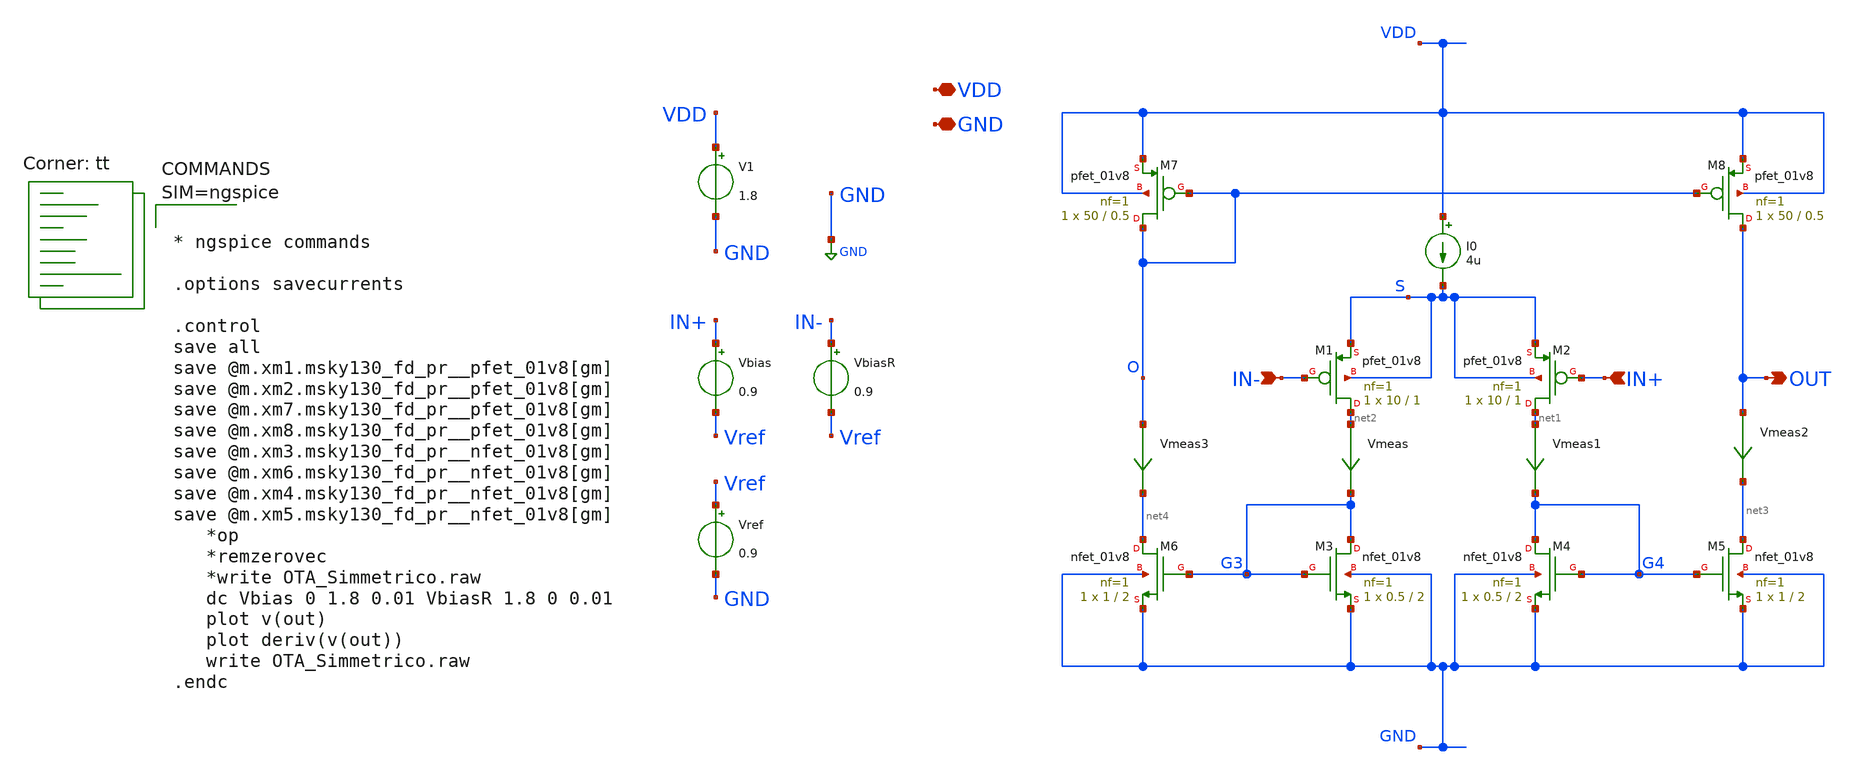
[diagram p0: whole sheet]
** sch_path: xschem/OTA_Simmetrico.sch
**.subckt OTA_Simmetrico VDD GND IN+ IN- OUT
*.iopin VDD
*.iopin GND
*.ipin IN+
*.ipin IN-
*.opin OUT
XM1 net2 IN- S S sky130_fd_pr__pfet_01v8 L=1 W=10 nf=1 ad='int((nf+1)/2) * W/nf * 0.29' as='int((nf+2)/2) * W/nf * 0.29'
+ pd='2*int((nf+1)/2) * (W/nf + 0.29)' ps='2*int((nf+2)/2) * (W/nf + 0.29)' nrd='0.29 / W' nrs='0.29 / W'
+ sa=0 sb=0 sd=0 mult=1 m=1
XM2 net1 IN+ S S sky130_fd_pr__pfet_01v8 L=1 W=10 nf=1 ad='int((nf+1)/2) * W/nf * 0.29' as='int((nf+2)/2) * W/nf * 0.29'
+ pd='2*int((nf+1)/2) * (W/nf + 0.29)' ps='2*int((nf+2)/2) * (W/nf + 0.29)' nrd='0.29 / W' nrs='0.29 / W'
+ sa=0 sb=0 sd=0 mult=1 m=1
XM3 G3 G3 GND GND sky130_fd_pr__nfet_01v8 L=2 W=0.5 nf=1 ad='int((nf+1)/2) * W/nf * 0.29' as='int((nf+2)/2) * W/nf * 0.29'
+ pd='2*int((nf+1)/2) * (W/nf + 0.29)' ps='2*int((nf+2)/2) * (W/nf + 0.29)' nrd='0.29 / W' nrs='0.29 / W'
+ sa=0 sb=0 sd=0 mult=1 m=1
XM4 G4 G4 GND GND sky130_fd_pr__nfet_01v8 L=2 W=0.5 nf=1 ad='int((nf+1)/2) * W/nf * 0.29' as='int((nf+2)/2) * W/nf * 0.29'
+ pd='2*int((nf+1)/2) * (W/nf + 0.29)' ps='2*int((nf+2)/2) * (W/nf + 0.29)' nrd='0.29 / W' nrs='0.29 / W'
+ sa=0 sb=0 sd=0 mult=1 m=1
XM5 net3 G4 GND GND sky130_fd_pr__nfet_01v8 L=2 W=1 nf=1 ad='int((nf+1)/2) * W/nf * 0.29' as='int((nf+2)/2) * W/nf * 0.29'
+ pd='2*int((nf+1)/2) * (W/nf + 0.29)' ps='2*int((nf+2)/2) * (W/nf + 0.29)' nrd='0.29 / W' nrs='0.29 / W'
+ sa=0 sb=0 sd=0 mult=1 m=1
XM6 net4 G3 GND GND sky130_fd_pr__nfet_01v8 L=2 W=1 nf=1 ad='int((nf+1)/2) * W/nf * 0.29' as='int((nf+2)/2) * W/nf * 0.29'
+ pd='2*int((nf+1)/2) * (W/nf + 0.29)' ps='2*int((nf+2)/2) * (W/nf + 0.29)' nrd='0.29 / W' nrs='0.29 / W'
+ sa=0 sb=0 sd=0 mult=1 m=1
XM7 O O VDD VDD sky130_fd_pr__pfet_01v8 L=0.5 W=50 nf=1 ad='int((nf+1)/2) * W/nf * 0.29' as='int((nf+2)/2) * W/nf * 0.29'
+ pd='2*int((nf+1)/2) * (W/nf + 0.29)' ps='2*int((nf+2)/2) * (W/nf + 0.29)' nrd='0.29 / W' nrs='0.29 / W'
+ sa=0 sb=0 sd=0 mult=1 m=1
XM8 OUT O VDD VDD sky130_fd_pr__pfet_01v8 L=0.5 W=50 nf=1 ad='int((nf+1)/2) * W/nf * 0.29' as='int((nf+2)/2) * W/nf * 0.29'
+ pd='2*int((nf+1)/2) * (W/nf + 0.29)' ps='2*int((nf+2)/2) * (W/nf + 0.29)' nrd='0.29 / W' nrs='0.29 / W'
+ sa=0 sb=0 sd=0 mult=1 m=1
I0 VDD S 4u
V1 VDD GND 1.8
Vbias IN+ Vref 0.9
VbiasR IN- Vref 0.9
Vmeas net2 G3 0
.save i(vmeas)
Vmeas1 net1 G4 0
.save i(vmeas1)
Vmeas2 OUT net3 0
.save i(vmeas2)
Vmeas3 O net4 0
.save i(vmeas3)
Vref Vref GND 0.9
**** begin user architecture code



* ngspice commands

.options savecurrents

.control
save all
save @m.xm1.msky130_fd_pr__pfet_01v8[gm]
save @m.xm2.msky130_fd_pr__pfet_01v8[gm]
save @m.xm7.msky130_fd_pr__pfet_01v8[gm]
save @m.xm8.msky130_fd_pr__pfet_01v8[gm]
save @m.xm3.msky130_fd_pr__nfet_01v8[gm]
save @m.xm6.msky130_fd_pr__nfet_01v8[gm]
save @m.xm4.msky130_fd_pr__nfet_01v8[gm]
save @m.xm5.msky130_fd_pr__nfet_01v8[gm]
   *op
   *remzerovec
   *write OTA_Simmetrico.raw
   dc Vbias 0 1.8 0.01 VbiasR 1.8 0 0.01
   plot v(out)
   plot deriv(v(out))
   write OTA_Simmetrico.raw
.endc




.lib $::SKYWATER_MODELS/sky130.lib.spice tt
**** end user architecture code
**.ends
.GLOBAL GND
.end
